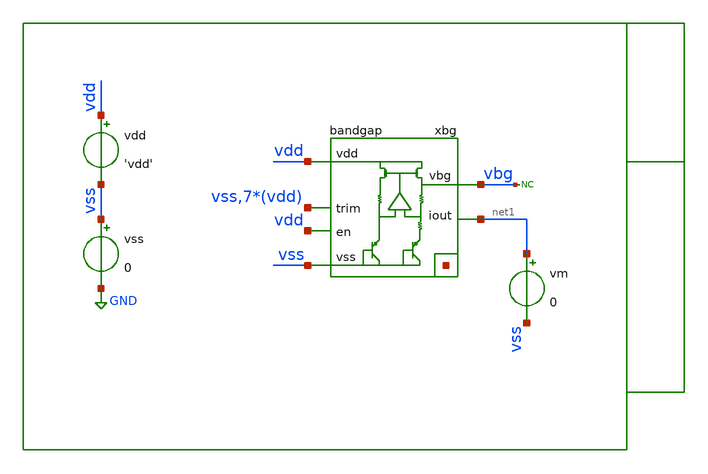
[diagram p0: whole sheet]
** sch_path: xschem/tb/bandgap_cm/bandgap/dc_bandgap_temperature.sch
**.subckt dc_bandgap_temperature
xbg vdd vbg vss net2[7] net2[6] net2[5] net2[4] net2[3] net2[2] net2[1] net2[0] vss vdd vdd vdd vdd
+ vdd vdd vdd net1 vdd bandgap
vdd vdd vss 'vdd'
vss vss GND 0
* noconn vbg
vm net1 vss 0
**** begin user architecture code

* Control

.param vdd = 3.3
.temp 27

.options reltol   = 1e-6
.options seed     = 3


.control
save all

dc temp -40 125 5
gnuplot p1 vbg

meas dc vbg_min min vbg from=0 to=75
meas dc vbg_max max vbg from=0 to=75

let vbg_min_eval = vbg_min + 1u
let vbg_max_eval = vbg_max - 1u

meas dc t_max when v(vbg)=vbg_max_eval
meas dc t_min when v(vbg)=vbg_min_eval

let dv_dT = (vbg_max-vbg_min)/abs((t_max-t_min))

let iout = abs(vm#branch)

gnuplot p2 iout

print vbg_min
print vbg_max
print t_min
print t_max
print dv_dT

.endc
.end


 * Model Corners

.include $::CORNERS/ngspice/tt.spice
*.include $::CORNERS/ngspice/ff.spice
*.include $::CORNERS/ngspice/ss.spice
*.include $::CORNERS/ngspice/sf.spice
*.include $::CORNERS/ngspice/fs.spice

 * extract

* tb_amplifier pex
*.include $::DESIGN_PATH/sch/bandgap_cm/bg_amplifier/bg_amplifier.pex.spice

* bandgap pex
*.include $::DESIGN_PATH/sch/bandgap_cm/bandgap/bandgap.pex.spice

**** end user architecture code
**.ends
.GLOBAL GND
.end
